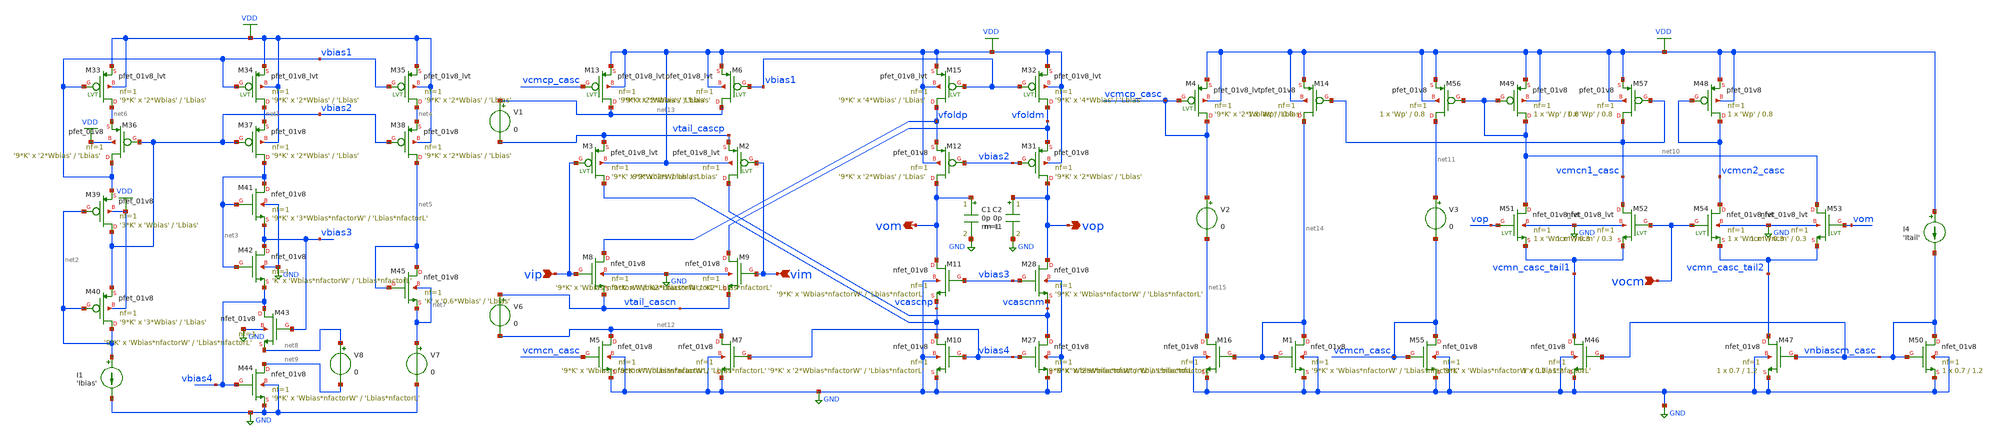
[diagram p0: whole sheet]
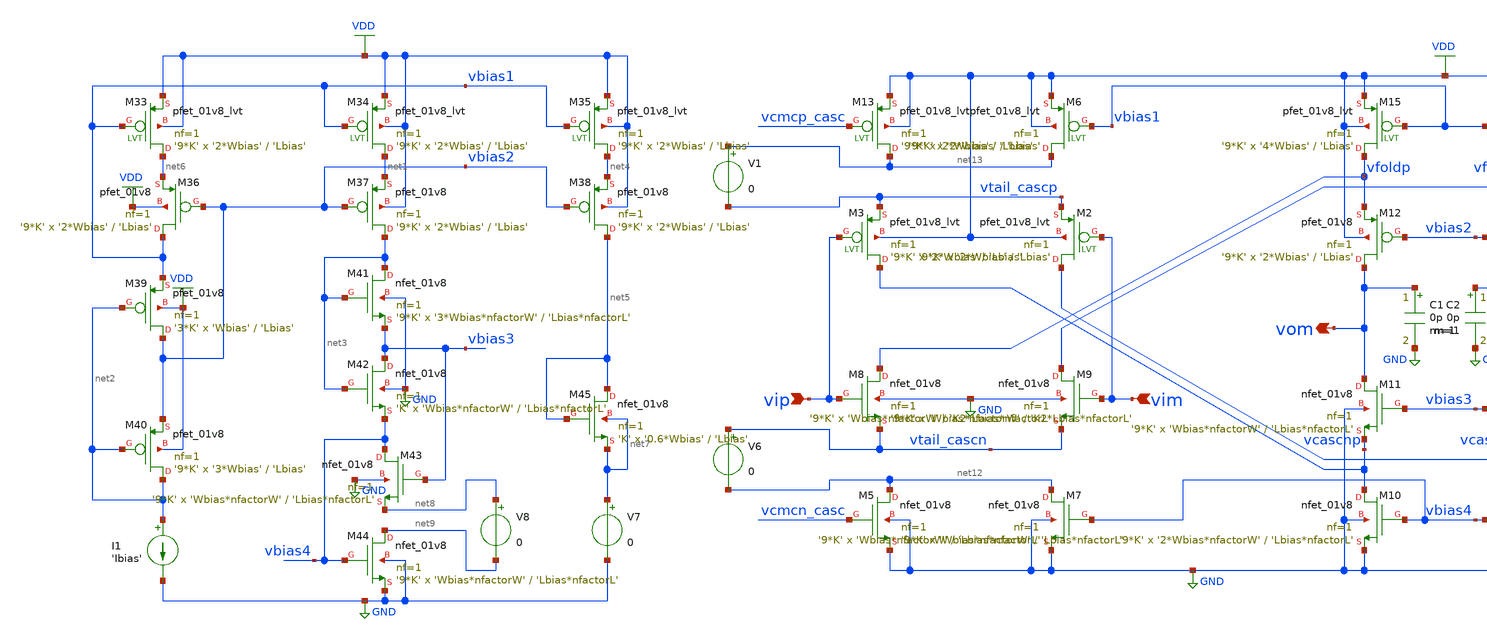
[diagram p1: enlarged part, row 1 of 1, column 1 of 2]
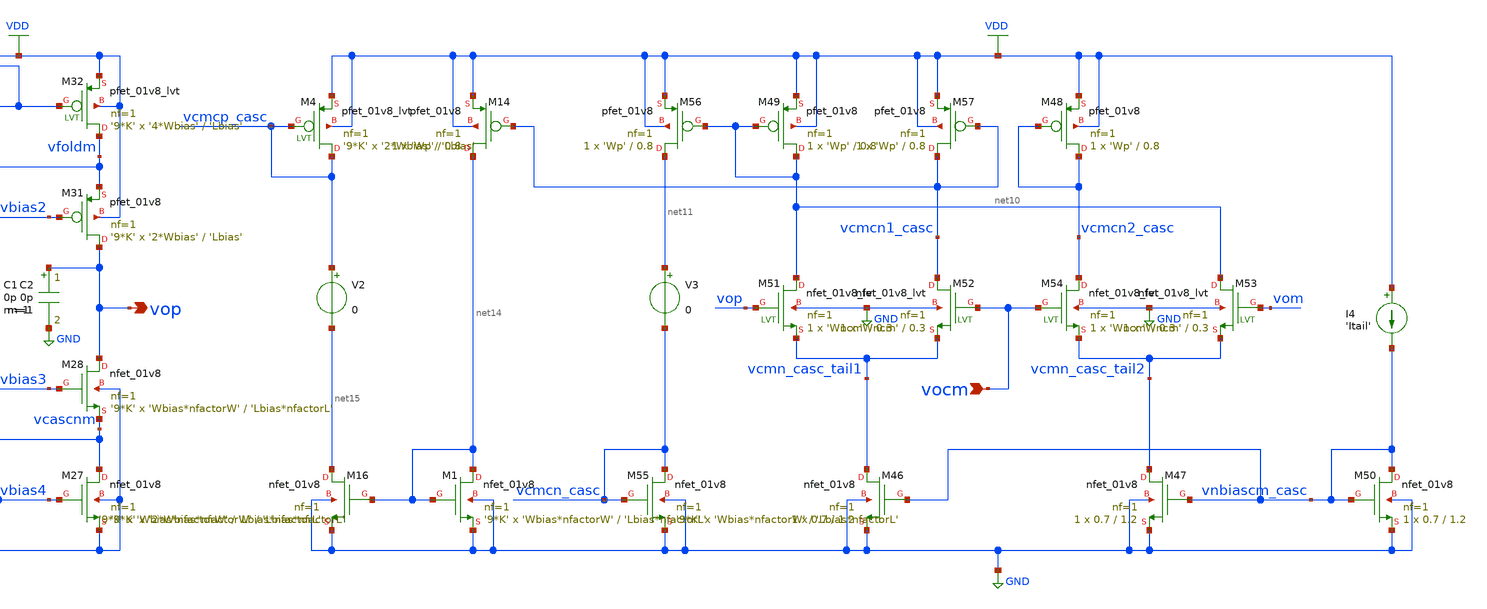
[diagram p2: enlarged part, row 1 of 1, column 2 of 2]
** sch_path: designs/diff_fold_casc_wide_swing_ota.sch
* Copyright 2020 Stefan Frederik Schippers
* Licensed under the Apache License, Version 2.0 (the "License");
* you may not use this file except in compliance with the License.
* You may obtain a copy of the License at
* https://www.apache.org/licenses/LICENSE-2.0
* Unless required by applicable law or agreed to in writing, software
* distributed under the License is distributed on an "AS IS" BASIS,
* WITHOUT WARRANTIES OR CONDITIONS OF ANY KIND, either express or implied.
* See the License for the specific language governing permissions and
* limitations under the License.
**.subckt diff_fold_casc_wide_swing_ota vocm vip vim vop vom
*.ipin vocm
*.ipin vip
*.ipin vim
*.opin vop
*.opin vom
XM36 vbias1 vbias2 net6 VDD sky130_fd_pr__pfet_01v8 L='Lbias' W='2*Wbias' nf=1 ad='int((nf+1)/2) * W/nf * 0.29'
+ as='int((nf+2)/2) * W/nf * 0.29' pd='2*int((nf+1)/2) * (W/nf + 0.29)' ps='2*int((nf+2)/2) * (W/nf + 0.29)'
+ nrd='0.29 / W' nrs='0.29 / W' sa=0 sb=0 sd=0 mult='9*K' m='9*K'
XM37 net3 vbias2 net1 VDD sky130_fd_pr__pfet_01v8 L='Lbias' W='2*Wbias' nf=1 ad='int((nf+1)/2) * W/nf * 0.29'
+ as='int((nf+2)/2) * W/nf * 0.29' pd='2*int((nf+1)/2) * (W/nf + 0.29)' ps='2*int((nf+2)/2) * (W/nf + 0.29)'
+ nrd='0.29 / W' nrs='0.29 / W' sa=0 sb=0 sd=0 mult='9*K' m='9*K'
XM38 net5 vbias2 net4 VDD sky130_fd_pr__pfet_01v8 L='Lbias' W='2*Wbias' nf=1 ad='int((nf+1)/2) * W/nf * 0.29'
+ as='int((nf+2)/2) * W/nf * 0.29' pd='2*int((nf+1)/2) * (W/nf + 0.29)' ps='2*int((nf+2)/2) * (W/nf + 0.29)'
+ nrd='0.29 / W' nrs='0.29 / W' sa=0 sb=0 sd=0 mult='9*K' m='9*K'
XM39 vbias2 net2 vbias1 VDD sky130_fd_pr__pfet_01v8 L='Lbias' W='Wbias' nf=1 ad='int((nf+1)/2) * W/nf * 0.29'
+ as='int((nf+2)/2) * W/nf * 0.29' pd='2*int((nf+1)/2) * (W/nf + 0.29)' ps='2*int((nf+2)/2) * (W/nf + 0.29)'
+ nrd='0.29 / W' nrs='0.29 / W' sa=0 sb=0 sd=0 mult='3*K' m='3*K'
XM40 net2 net2 vbias2 VDD sky130_fd_pr__pfet_01v8 L='Lbias' W='3*Wbias' nf=1 ad='int((nf+1)/2) * W/nf * 0.29'
+ as='int((nf+2)/2) * W/nf * 0.29' pd='2*int((nf+1)/2) * (W/nf + 0.29)' ps='2*int((nf+2)/2) * (W/nf + 0.29)'
+ nrd='0.29 / W' nrs='0.29 / W' sa=0 sb=0 sd=0 mult='9*K' m='9*K'
XM41 net3 net3 vbias3 GND sky130_fd_pr__nfet_01v8 L='Lbias*nfactorL' W='3*Wbias*nfactorW' nf=1 ad='int((nf+1)/2) * W/nf * 0.29'
+ as='int((nf+2)/2) * W/nf * 0.29' pd='2*int((nf+1)/2) * (W/nf + 0.29)' ps='2*int((nf+2)/2) * (W/nf + 0.29)'
+ nrd='0.29 / W' nrs='0.29 / W' sa=0 sb=0 sd=0 mult='9*K' m='9*K'
XM42 vbias3 net3 vbias4 GND sky130_fd_pr__nfet_01v8 L='Lbias*nfactorL' W='Wbias*nfactorW' nf=1 ad='int((nf+1)/2) * W/nf * 0.29'
+ as='int((nf+2)/2) * W/nf * 0.29' pd='2*int((nf+1)/2) * (W/nf + 0.29)' ps='2*int((nf+2)/2) * (W/nf + 0.29)'
+ nrd='0.29 / W' nrs='0.29 / W' sa=0 sb=0 sd=0 mult='K' m='K'
XM43 vbias4 vbias3 net8 GND sky130_fd_pr__nfet_01v8 L='Lbias*nfactorL' W='Wbias*nfactorW' nf=1 ad='int((nf+1)/2) * W/nf * 0.29'
+ as='int((nf+2)/2) * W/nf * 0.29' pd='2*int((nf+1)/2) * (W/nf + 0.29)' ps='2*int((nf+2)/2) * (W/nf + 0.29)'
+ nrd='0.29 / W' nrs='0.29 / W' sa=0 sb=0 sd=0 mult='9*K' m='9*K'
XM44 net9 vbias4 GND GND sky130_fd_pr__nfet_01v8 L='Lbias*nfactorL' W='Wbias*nfactorW' nf=1 ad='int((nf+1)/2) * W/nf * 0.29'
+ as='int((nf+2)/2) * W/nf * 0.29' pd='2*int((nf+1)/2) * (W/nf + 0.29)' ps='2*int((nf+2)/2) * (W/nf + 0.29)'
+ nrd='0.29 / W' nrs='0.29 / W' sa=0 sb=0 sd=0 mult='9*K' m='9*K'
XM45 net5 net5 net7 net7 sky130_fd_pr__nfet_01v8 L='Lbias' W='0.6*Wbias' nf=1 ad='int((nf+1)/2) * W/nf * 0.29'
+ as='int((nf+2)/2) * W/nf * 0.29' pd='2*int((nf+1)/2) * (W/nf + 0.29)' ps='2*int((nf+2)/2) * (W/nf + 0.29)'
+ nrd='0.29 / W' nrs='0.29 / W' sa=0 sb=0 sd=0 mult='K' m='K'
I1 net2 GND 'Ibias'
V7 net7 GND 0
V8 net8 net9 0
XM46 vcmn_casc_tail1 vnbiascm_casc GND GND sky130_fd_pr__nfet_01v8 L=1.2 W=0.7 nf=1 ad='int((nf+1)/2) * W/nf * 0.29'
+ as='int((nf+2)/2) * W/nf * 0.29' pd='2*int((nf+1)/2) * (W/nf + 0.29)' ps='2*int((nf+2)/2) * (W/nf + 0.29)'
+ nrd='0.29 / W' nrs='0.29 / W' sa=0 sb=0 sd=0 mult=1 m=1
XM47 vcmn_casc_tail2 vnbiascm_casc GND GND sky130_fd_pr__nfet_01v8 L=1.2 W=0.7 nf=1 ad='int((nf+1)/2) * W/nf * 0.29'
+ as='int((nf+2)/2) * W/nf * 0.29' pd='2*int((nf+1)/2) * (W/nf + 0.29)' ps='2*int((nf+2)/2) * (W/nf + 0.29)'
+ nrd='0.29 / W' nrs='0.29 / W' sa=0 sb=0 sd=0 mult=1 m=1
XM48 vcmcn2_casc vcmcn2_casc VDD VDD sky130_fd_pr__pfet_01v8 L=0.8 W='Wp' nf=1 ad='int((nf+1)/2) * W/nf * 0.29'
+ as='int((nf+2)/2) * W/nf * 0.29' pd='2*int((nf+1)/2) * (W/nf + 0.29)' ps='2*int((nf+2)/2) * (W/nf + 0.29)'
+ nrd='0.29 / W' nrs='0.29 / W' sa=0 sb=0 sd=0 mult=1 m=1
XM49 net10 net10 VDD VDD sky130_fd_pr__pfet_01v8 L=0.8 W='Wp' nf=1 ad='int((nf+1)/2) * W/nf * 0.29' as='int((nf+2)/2) * W/nf * 0.29'
+ pd='2*int((nf+1)/2) * (W/nf + 0.29)' ps='2*int((nf+2)/2) * (W/nf + 0.29)' nrd='0.29 / W' nrs='0.29 / W'
+ sa=0 sb=0 sd=0 mult=1 m=1
I4 VDD vnbiascm_casc 'Itail'
XM50 vnbiascm_casc vnbiascm_casc GND GND sky130_fd_pr__nfet_01v8 L=1.2 W=0.7 nf=1 ad='int((nf+1)/2) * W/nf * 0.29'
+ as='int((nf+2)/2) * W/nf * 0.29' pd='2*int((nf+1)/2) * (W/nf + 0.29)' ps='2*int((nf+2)/2) * (W/nf + 0.29)'
+ nrd='0.29 / W' nrs='0.29 / W' sa=0 sb=0 sd=0 mult=1 m=1
XM51 net10 vop vcmn_casc_tail1 GND sky130_fd_pr__nfet_01v8_lvt L=0.3 W='Wncm' nf=1 ad='int((nf+1)/2) * W/nf * 0.29'
+ as='int((nf+2)/2) * W/nf * 0.29' pd='2*int((nf+1)/2) * (W/nf + 0.29)' ps='2*int((nf+2)/2) * (W/nf + 0.29)'
+ nrd='0.29 / W' nrs='0.29 / W' sa=0 sb=0 sd=0 mult=1 m=1
XM52 vcmcn1_casc vocm vcmn_casc_tail1 GND sky130_fd_pr__nfet_01v8_lvt L=0.3 W='Wncm' nf=1 ad='int((nf+1)/2) * W/nf * 0.29'
+ as='int((nf+2)/2) * W/nf * 0.29' pd='2*int((nf+1)/2) * (W/nf + 0.29)' ps='2*int((nf+2)/2) * (W/nf + 0.29)'
+ nrd='0.29 / W' nrs='0.29 / W' sa=0 sb=0 sd=0 mult=1 m=1
XM53 net10 vom vcmn_casc_tail2 GND sky130_fd_pr__nfet_01v8_lvt L=0.3 W='Wncm' nf=1 ad='int((nf+1)/2) * W/nf * 0.29'
+ as='int((nf+2)/2) * W/nf * 0.29' pd='2*int((nf+1)/2) * (W/nf + 0.29)' ps='2*int((nf+2)/2) * (W/nf + 0.29)'
+ nrd='0.29 / W' nrs='0.29 / W' sa=0 sb=0 sd=0 mult=1 m=1
XM54 vcmcn2_casc vocm vcmn_casc_tail2 GND sky130_fd_pr__nfet_01v8_lvt L=0.3 W='Wncm' nf=1 ad='int((nf+1)/2) * W/nf * 0.29'
+ as='int((nf+2)/2) * W/nf * 0.29' pd='2*int((nf+1)/2) * (W/nf + 0.29)' ps='2*int((nf+2)/2) * (W/nf + 0.29)'
+ nrd='0.29 / W' nrs='0.29 / W' sa=0 sb=0 sd=0 mult=1 m=1
XM56 net11 net10 VDD VDD sky130_fd_pr__pfet_01v8 L=0.8 W='Wp' nf=1 ad='int((nf+1)/2) * W/nf * 0.29' as='int((nf+2)/2) * W/nf * 0.29'
+ pd='2*int((nf+1)/2) * (W/nf + 0.29)' ps='2*int((nf+2)/2) * (W/nf + 0.29)' nrd='0.29 / W' nrs='0.29 / W'
+ sa=0 sb=0 sd=0 mult=1 m=1
XM57 vcmcn1_casc vcmcn1_casc VDD VDD sky130_fd_pr__pfet_01v8 L=0.8 W='Wp' nf=1 ad='int((nf+1)/2) * W/nf * 0.29'
+ as='int((nf+2)/2) * W/nf * 0.29' pd='2*int((nf+1)/2) * (W/nf + 0.29)' ps='2*int((nf+2)/2) * (W/nf + 0.29)'
+ nrd='0.29 / W' nrs='0.29 / W' sa=0 sb=0 sd=0 mult=1 m=1
XM33 net6 vbias1 VDD VDD sky130_fd_pr__pfet_01v8_lvt L='Lbias' W='2*Wbias' nf=1 ad='int((nf+1)/2) * W/nf * 0.29'
+ as='int((nf+2)/2) * W/nf * 0.29' pd='2*int((nf+1)/2) * (W/nf + 0.29)' ps='2*int((nf+2)/2) * (W/nf + 0.29)'
+ nrd='0.29 / W' nrs='0.29 / W' sa=0 sb=0 sd=0 mult='9*K' m='9*K'
XM34 net1 vbias1 VDD VDD sky130_fd_pr__pfet_01v8_lvt L='Lbias' W='2*Wbias' nf=1 ad='int((nf+1)/2) * W/nf * 0.29'
+ as='int((nf+2)/2) * W/nf * 0.29' pd='2*int((nf+1)/2) * (W/nf + 0.29)' ps='2*int((nf+2)/2) * (W/nf + 0.29)'
+ nrd='0.29 / W' nrs='0.29 / W' sa=0 sb=0 sd=0 mult='9*K' m='9*K'
XM35 net4 vbias1 VDD VDD sky130_fd_pr__pfet_01v8_lvt L='Lbias' W='2*Wbias' nf=1 ad='int((nf+1)/2) * W/nf * 0.29'
+ as='int((nf+2)/2) * W/nf * 0.29' pd='2*int((nf+1)/2) * (W/nf + 0.29)' ps='2*int((nf+2)/2) * (W/nf + 0.29)'
+ nrd='0.29 / W' nrs='0.29 / W' sa=0 sb=0 sd=0 mult='9*K' m='9*K'
XM55 vcmcn_casc vcmcn_casc GND GND sky130_fd_pr__nfet_01v8 L='Lbias*nfactorL' W='Wbias*nfactorW' nf=1
+ ad='int((nf+1)/2) * W/nf * 0.29' as='int((nf+2)/2) * W/nf * 0.29' pd='2*int((nf+1)/2) * (W/nf + 0.29)'
+ ps='2*int((nf+2)/2) * (W/nf + 0.29)' nrd='0.29 / W' nrs='0.29 / W' sa=0 sb=0 sd=0 mult='9*K' m='9*K'
V6 vtail_cascn net12 0
XM7 net12 vbias4 GND GND sky130_fd_pr__nfet_01v8 L='Lbias*nfactorL' W='Wbias*nfactorW' nf=1 ad='int((nf+1)/2) * W/nf * 0.29'
+ as='int((nf+2)/2) * W/nf * 0.29' pd='2*int((nf+1)/2) * (W/nf + 0.29)' ps='2*int((nf+2)/2) * (W/nf + 0.29)'
+ nrd='0.29 / W' nrs='0.29 / W' sa=0 sb=0 sd=0 mult='9*K' m='9*K'
XM10 vcascnp vbias4 GND GND sky130_fd_pr__nfet_01v8 L='Lbias*nfactorL' W='2*Wbias*nfactorW' nf=1 ad='int((nf+1)/2) * W/nf * 0.29'
+ as='int((nf+2)/2) * W/nf * 0.29' pd='2*int((nf+1)/2) * (W/nf + 0.29)' ps='2*int((nf+2)/2) * (W/nf + 0.29)'
+ nrd='0.29 / W' nrs='0.29 / W' sa=0 sb=0 sd=0 mult='9*K' m='9*K'
XM11 vom vbias3 vcascnp GND sky130_fd_pr__nfet_01v8 L='Lbias*nfactorL' W='Wbias*nfactorW' nf=1 ad='int((nf+1)/2) * W/nf * 0.29'
+ as='int((nf+2)/2) * W/nf * 0.29' pd='2*int((nf+1)/2) * (W/nf + 0.29)' ps='2*int((nf+2)/2) * (W/nf + 0.29)'
+ nrd='0.29 / W' nrs='0.29 / W' sa=0 sb=0 sd=0 mult='9*K' m='9*K'
XM27 vcascnm vbias4 GND GND sky130_fd_pr__nfet_01v8 L='Lbias*nfactorL' W='2*Wbias*nfactorW' nf=1 ad='int((nf+1)/2) * W/nf * 0.29'
+ as='int((nf+2)/2) * W/nf * 0.29' pd='2*int((nf+1)/2) * (W/nf + 0.29)' ps='2*int((nf+2)/2) * (W/nf + 0.29)'
+ nrd='0.29 / W' nrs='0.29 / W' sa=0 sb=0 sd=0 mult='9*K' m='9*K'
XM28 vop vbias3 vcascnm GND sky130_fd_pr__nfet_01v8 L='Lbias*nfactorL' W='Wbias*nfactorW' nf=1 ad='int((nf+1)/2) * W/nf * 0.29'
+ as='int((nf+2)/2) * W/nf * 0.29' pd='2*int((nf+1)/2) * (W/nf + 0.29)' ps='2*int((nf+2)/2) * (W/nf + 0.29)'
+ nrd='0.29 / W' nrs='0.29 / W' sa=0 sb=0 sd=0 mult='9*K' m='9*K'
XM8 vfoldp vip vtail_cascn GND sky130_fd_pr__nfet_01v8 L='K2*Lbias*nfactorL' W='Wbias*nfactorW' nf=1
+ ad='int((nf+1)/2) * W/nf * 0.29' as='int((nf+2)/2) * W/nf * 0.29' pd='2*int((nf+1)/2) * (W/nf + 0.29)'
+ ps='2*int((nf+2)/2) * (W/nf + 0.29)' nrd='0.29 / W' nrs='0.29 / W' sa=0 sb=0 sd=0 mult='9*K' m='9*K'
XM12 vom vbias2 vfoldp VDD sky130_fd_pr__pfet_01v8 L='Lbias' W='2*Wbias' nf=1 ad='int((nf+1)/2) * W/nf * 0.29'
+ as='int((nf+2)/2) * W/nf * 0.29' pd='2*int((nf+1)/2) * (W/nf + 0.29)' ps='2*int((nf+2)/2) * (W/nf + 0.29)'
+ nrd='0.29 / W' nrs='0.29 / W' sa=0 sb=0 sd=0 mult='9*K' m='9*K'
XM31 vop vbias2 vfoldm VDD sky130_fd_pr__pfet_01v8 L='Lbias' W='2*Wbias' nf=1 ad='int((nf+1)/2) * W/nf * 0.29'
+ as='int((nf+2)/2) * W/nf * 0.29' pd='2*int((nf+1)/2) * (W/nf + 0.29)' ps='2*int((nf+2)/2) * (W/nf + 0.29)'
+ nrd='0.29 / W' nrs='0.29 / W' sa=0 sb=0 sd=0 mult='9*K' m='9*K'
XM15 vfoldp vbias1 VDD VDD sky130_fd_pr__pfet_01v8_lvt L='Lbias' W='4*Wbias' nf=1 ad='int((nf+1)/2) * W/nf * 0.29'
+ as='int((nf+2)/2) * W/nf * 0.29' pd='2*int((nf+1)/2) * (W/nf + 0.29)' ps='2*int((nf+2)/2) * (W/nf + 0.29)'
+ nrd='0.29 / W' nrs='0.29 / W' sa=0 sb=0 sd=0 mult='9*K' m='9*K'
XM32 vfoldm vbias1 VDD VDD sky130_fd_pr__pfet_01v8_lvt L='Lbias' W='4*Wbias' nf=1 ad='int((nf+1)/2) * W/nf * 0.29'
+ as='int((nf+2)/2) * W/nf * 0.29' pd='2*int((nf+1)/2) * (W/nf + 0.29)' ps='2*int((nf+2)/2) * (W/nf + 0.29)'
+ nrd='0.29 / W' nrs='0.29 / W' sa=0 sb=0 sd=0 mult='9*K' m='9*K'
XM5 net12 vcmcn_casc GND GND sky130_fd_pr__nfet_01v8 L='Lbias*nfactorL' W='Wbias*nfactorW' nf=1 ad='int((nf+1)/2) * W/nf * 0.29'
+ as='int((nf+2)/2) * W/nf * 0.29' pd='2*int((nf+1)/2) * (W/nf + 0.29)' ps='2*int((nf+2)/2) * (W/nf + 0.29)'
+ nrd='0.29 / W' nrs='0.29 / W' sa=0 sb=0 sd=0 mult='9*K' m='9*K'
XM9 vfoldm vim vtail_cascn GND sky130_fd_pr__nfet_01v8 L='K2*Lbias*nfactorL' W='Wbias*nfactorW' nf=1
+ ad='int((nf+1)/2) * W/nf * 0.29' as='int((nf+2)/2) * W/nf * 0.29' pd='2*int((nf+1)/2) * (W/nf + 0.29)'
+ ps='2*int((nf+2)/2) * (W/nf + 0.29)' nrd='0.29 / W' nrs='0.29 / W' sa=0 sb=0 sd=0 mult='9*K' m='9*K'
XM6 net13 vbias1 VDD VDD sky130_fd_pr__pfet_01v8_lvt L='Lbias' W='2*Wbias' nf=1 ad='int((nf+1)/2) * W/nf * 0.29'
+ as='int((nf+2)/2) * W/nf * 0.29' pd='2*int((nf+1)/2) * (W/nf + 0.29)' ps='2*int((nf+2)/2) * (W/nf + 0.29)'
+ nrd='0.29 / W' nrs='0.29 / W' sa=0 sb=0 sd=0 mult='9*K' m='9*K'
V1 net13 vtail_cascp 0
XM13 net13 vcmcp_casc VDD VDD sky130_fd_pr__pfet_01v8_lvt L='Lbias' W='2*Wbias' nf=1 ad='int((nf+1)/2) * W/nf * 0.29'
+ as='int((nf+2)/2) * W/nf * 0.29' pd='2*int((nf+1)/2) * (W/nf + 0.29)' ps='2*int((nf+2)/2) * (W/nf + 0.29)'
+ nrd='0.29 / W' nrs='0.29 / W' sa=0 sb=0 sd=0 mult='9*K' m='9*K'
XM2 vcascnm vim vtail_cascp VDD sky130_fd_pr__pfet_01v8_lvt L='Lbias' W='2*Wbias' nf=1 ad='int((nf+1)/2) * W/nf * 0.29'
+ as='int((nf+2)/2) * W/nf * 0.29' pd='2*int((nf+1)/2) * (W/nf + 0.29)' ps='2*int((nf+2)/2) * (W/nf + 0.29)'
+ nrd='0.29 / W' nrs='0.29 / W' sa=0 sb=0 sd=0 mult='9*K' m='9*K'
XM3 vcascnp vip vtail_cascp VDD sky130_fd_pr__pfet_01v8_lvt L='Lbias' W='2*Wbias' nf=1 ad='int((nf+1)/2) * W/nf * 0.29'
+ as='int((nf+2)/2) * W/nf * 0.29' pd='2*int((nf+1)/2) * (W/nf + 0.29)' ps='2*int((nf+2)/2) * (W/nf + 0.29)'
+ nrd='0.29 / W' nrs='0.29 / W' sa=0 sb=0 sd=0 mult='9*K' m='9*K'
C2 vop GND 0p m=1
C1 vom GND 0p m=1
XM4 vcmcp_casc vcmcp_casc VDD VDD sky130_fd_pr__pfet_01v8_lvt L='Lbias' W='2*Wbias' nf=1 ad='int((nf+1)/2) * W/nf * 0.29'
+ as='int((nf+2)/2) * W/nf * 0.29' pd='2*int((nf+1)/2) * (W/nf + 0.29)' ps='2*int((nf+2)/2) * (W/nf + 0.29)'
+ nrd='0.29 / W' nrs='0.29 / W' sa=0 sb=0 sd=0 mult='9*K' m='9*K'
XM14 net14 vcmcn1_casc VDD VDD sky130_fd_pr__pfet_01v8 L=0.8 W='Wp' nf=1 ad='int((nf+1)/2) * W/nf * 0.29'
+ as='int((nf+2)/2) * W/nf * 0.29' pd='2*int((nf+1)/2) * (W/nf + 0.29)' ps='2*int((nf+2)/2) * (W/nf + 0.29)'
+ nrd='0.29 / W' nrs='0.29 / W' sa=0 sb=0 sd=0 mult=1 m=1
XM1 net14 net14 GND GND sky130_fd_pr__nfet_01v8 L='Lbias*nfactorL' W='Wbias*nfactorW' nf=1 ad='int((nf+1)/2) * W/nf * 0.29'
+ as='int((nf+2)/2) * W/nf * 0.29' pd='2*int((nf+1)/2) * (W/nf + 0.29)' ps='2*int((nf+2)/2) * (W/nf + 0.29)'
+ nrd='0.29 / W' nrs='0.29 / W' sa=0 sb=0 sd=0 mult='9*K' m='9*K'
XM16 net15 net14 GND GND sky130_fd_pr__nfet_01v8 L='Lbias*nfactorL' W='Wbias*nfactorW' nf=1 ad='int((nf+1)/2) * W/nf * 0.29'
+ as='int((nf+2)/2) * W/nf * 0.29' pd='2*int((nf+1)/2) * (W/nf + 0.29)' ps='2*int((nf+2)/2) * (W/nf + 0.29)'
+ nrd='0.29 / W' nrs='0.29 / W' sa=0 sb=0 sd=0 mult='9*K' m='9*K'
V2 vcmcp_casc net15 0
V3 net11 vcmcn_casc 0
**** begin user architecture code

.include $::SKYWATER_MODELS/cells/nfet_01v8/sky130_fd_pr__nfet_01v8__tt.corner.spice
.include $::SKYWATER_MODELS/cells/nfet_01v8_lvt/sky130_fd_pr__nfet_01v8_lvt__tt.corner.spice
.include $::SKYWATER_MODELS/cells/pfet_01v8/sky130_fd_pr__pfet_01v8__tt.corner.spice
.include $::SKYWATER_MODELS/cells/nfet_03v3_nvt/sky130_fd_pr__nfet_03v3_nvt__tt.corner.spice
.include $::SKYWATER_MODELS/cells/nfet_05v0_nvt/sky130_fd_pr__nfet_05v0_nvt__tt.corner.spice
.include $::SKYWATER_MODELS/cells/esd_nfet_01v8/sky130_fd_pr__esd_nfet_01v8__tt.corner.spice
.include $::SKYWATER_MODELS/cells/pfet_01v8_lvt/sky130_fd_pr__pfet_01v8_lvt__tt.corner.spice
.include $::SKYWATER_MODELS/cells/pfet_01v8_hvt/sky130_fd_pr__pfet_01v8_hvt__tt.corner.spice
.include $::SKYWATER_MODELS/cells/esd_pfet_g5v0d10v5/sky130_fd_pr__esd_pfet_g5v0d10v5__tt.corner.spice
.include $::SKYWATER_MODELS/cells/pfet_g5v0d10v5/sky130_fd_pr__pfet_g5v0d10v5__tt.corner.spice
.include $::SKYWATER_MODELS/cells/pfet_g5v0d16v0/sky130_fd_pr__pfet_g5v0d16v0__tt.corner.spice
.include $::SKYWATER_MODELS/cells/nfet_g5v0d10v5/sky130_fd_pr__nfet_g5v0d10v5__tt.corner.spice
.include $::SKYWATER_MODELS/cells/nfet_g5v0d16v0/sky130_fd_pr__nfet_g5v0d16v0__tt_discrete.corner.spice
.include $::SKYWATER_MODELS/cells/esd_nfet_g5v0d10v5/sky130_fd_pr__esd_nfet_g5v0d10v5__tt.corner.spice
.include $::SKYWATER_MODELS/models/corners/tt/nonfet.spice
* Mismatch parameters
.include $::SKYWATER_MODELS/cells/nfet_01v8/sky130_fd_pr__nfet_01v8__mismatch.corner.spice
.include $::SKYWATER_MODELS/cells/pfet_01v8/sky130_fd_pr__pfet_01v8__mismatch.corner.spice
.include $::SKYWATER_MODELS/cells/nfet_01v8_lvt/sky130_fd_pr__nfet_01v8_lvt__mismatch.corner.spice
.include $::SKYWATER_MODELS/cells/pfet_01v8_lvt/sky130_fd_pr__pfet_01v8_lvt__mismatch.corner.spice
.include $::SKYWATER_MODELS/cells/pfet_01v8_hvt/sky130_fd_pr__pfet_01v8_hvt__mismatch.corner.spice
.include $::SKYWATER_MODELS/cells/nfet_g5v0d10v5/sky130_fd_pr__nfet_g5v0d10v5__mismatch.corner.spice
.include $::SKYWATER_MODELS/cells/pfet_g5v0d10v5/sky130_fd_pr__pfet_g5v0d10v5__mismatch.corner.spice
.include $::SKYWATER_MODELS/cells/nfet_05v0_nvt/sky130_fd_pr__nfet_05v0_nvt__mismatch.corner.spice
.include $::SKYWATER_MODELS/cells/nfet_03v3_nvt/sky130_fd_pr__nfet_03v3_nvt__mismatch.corner.spice
* Resistor$::SKYWATER_MODELS/Capacitor
.include $::SKYWATER_MODELS/models/r+c/res_typical__cap_typical.spice
.include $::SKYWATER_MODELS/models/r+c/res_typical__cap_typical__lin.spice
* Special cells
.include $::SKYWATER_MODELS/models/corners/tt/specialized_cells.spice
* All models
.include $::SKYWATER_MODELS/models/all.spice
* Corner
.include $::SKYWATER_MODELS/models/corners/tt/rf.spice

**** end user architecture code
**.ends
.GLOBAL GND
.GLOBAL VDD
**** begin user architecture code

.include diff_fold_casc_wide_swing_ota_commands.spice

**** end user architecture code
.end
